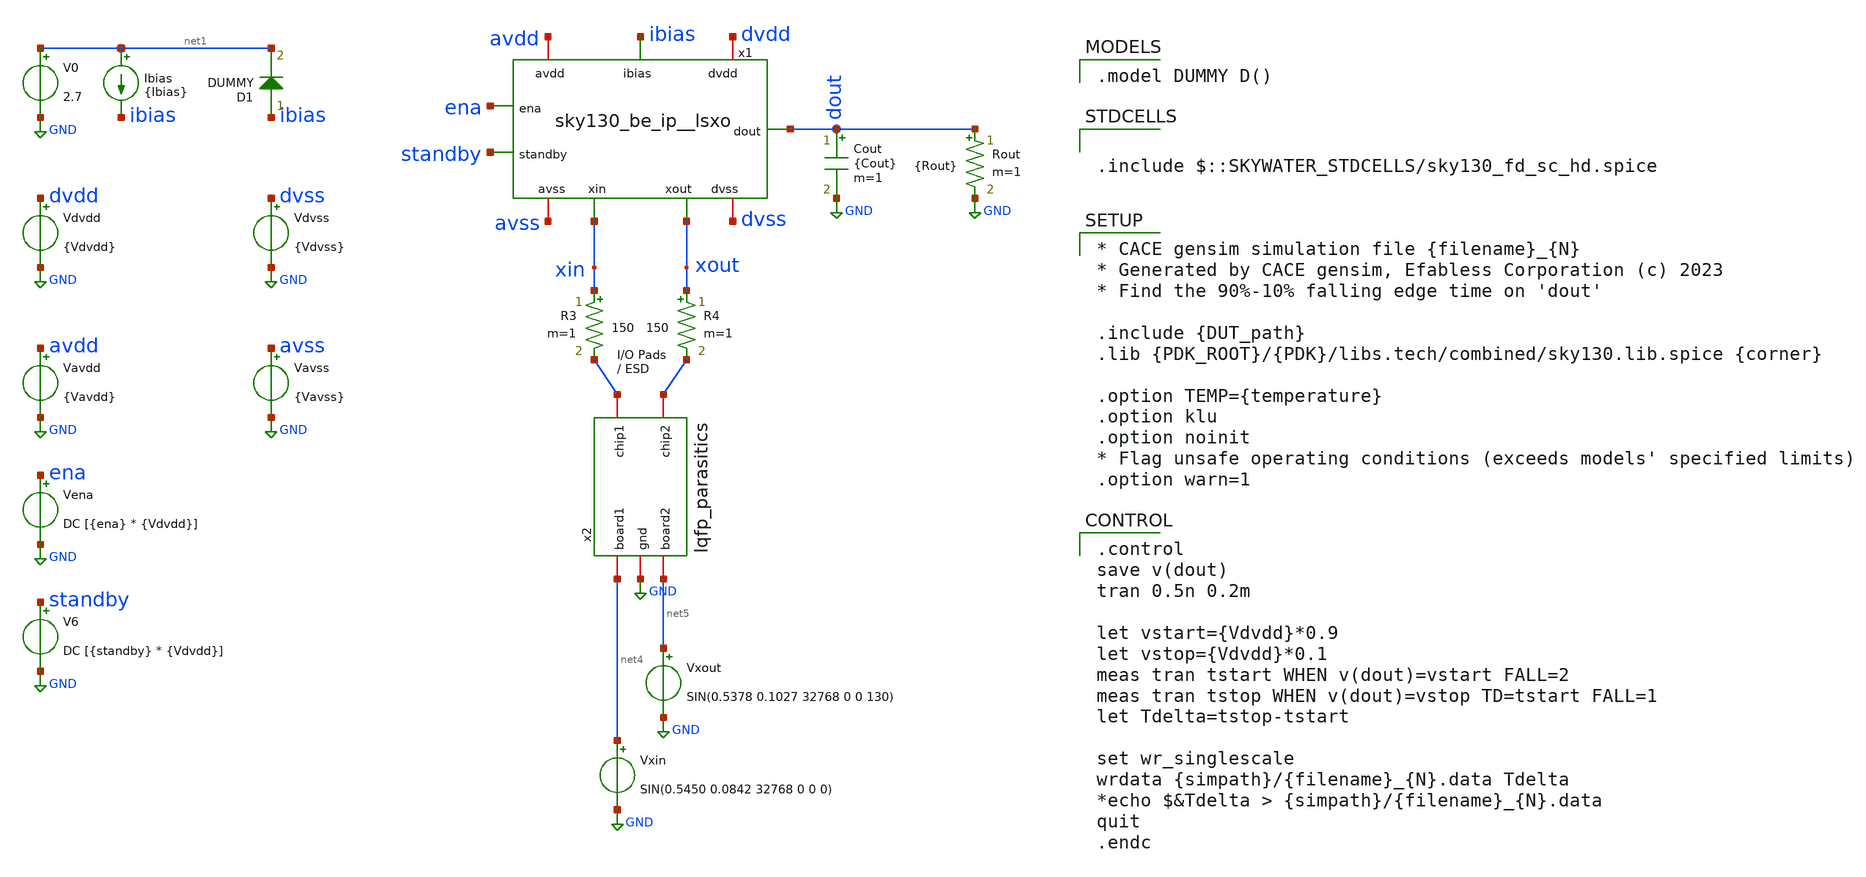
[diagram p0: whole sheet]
** sch_path: cace/tb_fall.sch

.include $::SKYWATER_STDCELLS/sky130_fd_sc_hd.spice

**.subckt tb_fall
Vdvdd dvdd GND {Vdvdd}
Vavdd avdd GND {Vavdd}
Ibias net1 ibias {Ibias}
Cout dout GND {Cout} m=1
V0 net1 GND 2.7
V6 standby GND DC [{standby} * {Vdvdd}]
R3 xin net2 150 m=1
R4 xout net3 150 m=1
x2 net3 net2 GND net4 net5 lqfp_parasitics
Vena ena GND DC [{ena} * {Vdvdd}]
D1 ibias net1 DUMMY area=100
x1 avdd avss dvdd dvss ibias ena standby dout xin xout sky130_be_ip__lsxo
Vdvss dvss GND {Vdvss}
Vavss avss GND {Vavss}
Rout dout GND {Rout} m=1
Vxout net5 GND SIN(0.5378 0.1027 32768 0 0 130)
Vxin net4 GND SIN(0.5450 0.0842 32768 0 0 0)
**** begin user architecture code

.model DUMMY D()


.control
save v(dout)
tran 0.5n 0.2m

let vstart={Vdvdd}*0.9
let vstop={Vdvdd}*0.1
meas tran tstart WHEN v(dout)=vstart FALL=2
meas tran tstop WHEN v(dout)=vstop TD=tstart FALL=1
let Tdelta=tstop-tstart

set wr_singlescale
wrdata {simpath}/{filename}_{N}.data Tdelta
*echo $&Tdelta > {simpath}/{filename}_{N}.data
quit
.endc



* CACE gensim simulation file {filename}_{N}
* Generated by CACE gensim, Efabless Corporation (c) 2023
* Find the 90%-10% falling edge time on 'dout'

.include {DUT_path}
.lib {PDK_ROOT}/{PDK}/libs.tech/combined/sky130.lib.spice {corner}

.option TEMP={temperature}
.option klu
.option noinit
* Flag unsafe operating conditions (exceeds models' specified limits)
.option warn=1


**** end user architecture code
**.ends
.GLOBAL GND
.end
